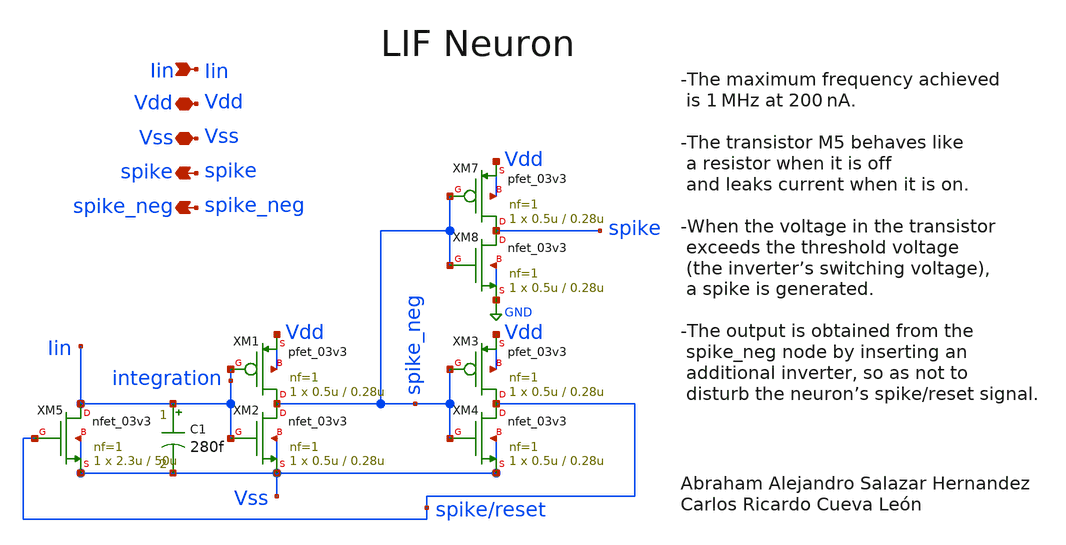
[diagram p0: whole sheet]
** sch_path: designs/libs/snn_analog/lif/sch/lif/neurona.sch
**.subckt neurona Vdd Vss Iin spike spike_neg
*.iopin Vdd
*.iopin Vss
*.ipin Iin
*.opin spike
*.opin spike_neg
XM1 spike_neg integration Vdd Vdd pfet_03v3 L=0.28u W=0.5u nf=1 ad='int((nf+1)/2) * W/nf * 0.18u' as='int((nf+2)/2) * W/nf * 0.18u'
+ pd='2*int((nf+1)/2) * (W/nf + 0.18u)' ps='2*int((nf+2)/2) * (W/nf + 0.18u)' nrd='0.18u / W' nrs='0.18u / W'
+ sa=0 sb=0 sd=0 m=1
XM2 spike_neg integration Vss Vss nfet_03v3 L=0.28u W=0.5u nf=1 ad='int((nf+1)/2) * W/nf * 0.18u' as='int((nf+2)/2) * W/nf * 0.18u'
+ pd='2*int((nf+1)/2) * (W/nf + 0.18u)' ps='2*int((nf+2)/2) * (W/nf + 0.18u)' nrd='0.18u / W' nrs='0.18u / W'
+ sa=0 sb=0 sd=0 m=1
XM3 spike/reset spike_neg Vdd Vdd pfet_03v3 L=0.28u W=0.5u nf=1 ad='int((nf+1)/2) * W/nf * 0.18u' as='int((nf+2)/2) * W/nf * 0.18u'
+ pd='2*int((nf+1)/2) * (W/nf + 0.18u)' ps='2*int((nf+2)/2) * (W/nf + 0.18u)' nrd='0.18u / W' nrs='0.18u / W'
+ sa=0 sb=0 sd=0 m=1
XM4 spike/reset spike_neg Vss Vss nfet_03v3 L=0.28u W=0.5u nf=1 ad='int((nf+1)/2) * W/nf * 0.18u' as='int((nf+2)/2) * W/nf * 0.18u'
+ pd='2*int((nf+1)/2) * (W/nf + 0.18u)' ps='2*int((nf+2)/2) * (W/nf + 0.18u)' nrd='0.18u / W' nrs='0.18u / W'
+ sa=0 sb=0 sd=0 m=1
XM7 spike spike_neg Vdd Vdd pfet_03v3 L=0.28u W=0.5u nf=1 ad='int((nf+1)/2) * W/nf * 0.18u' as='int((nf+2)/2) * W/nf * 0.18u'
+ pd='2*int((nf+1)/2) * (W/nf + 0.18u)' ps='2*int((nf+2)/2) * (W/nf + 0.18u)' nrd='0.18u / W' nrs='0.18u / W'
+ sa=0 sb=0 sd=0 m=1
XM8 spike spike_neg GND GND nfet_03v3 L=0.28u W=0.5u nf=1 ad='int((nf+1)/2) * W/nf * 0.18u' as='int((nf+2)/2) * W/nf * 0.18u'
+ pd='2*int((nf+1)/2) * (W/nf + 0.18u)' ps='2*int((nf+2)/2) * (W/nf + 0.18u)' nrd='0.18u / W' nrs='0.18u / W'
+ sa=0 sb=0 sd=0 m=1
XM5 integration spike/reset Vss Vss nfet_03v3 L=50u W=2.3u nf=1 ad='int((nf+1)/2) * W/nf * 0.18u' as='int((nf+2)/2) * W/nf * 0.18u'
+ pd='2*int((nf+1)/2) * (W/nf + 0.18u)' ps='2*int((nf+2)/2) * (W/nf + 0.18u)' nrd='0.18u / W' nrs='0.18u / W'
+ sa=0 sb=0 sd=0 m=1
C1 integration Vss 280f m=1
**.ends
.GLOBAL GND
.end
